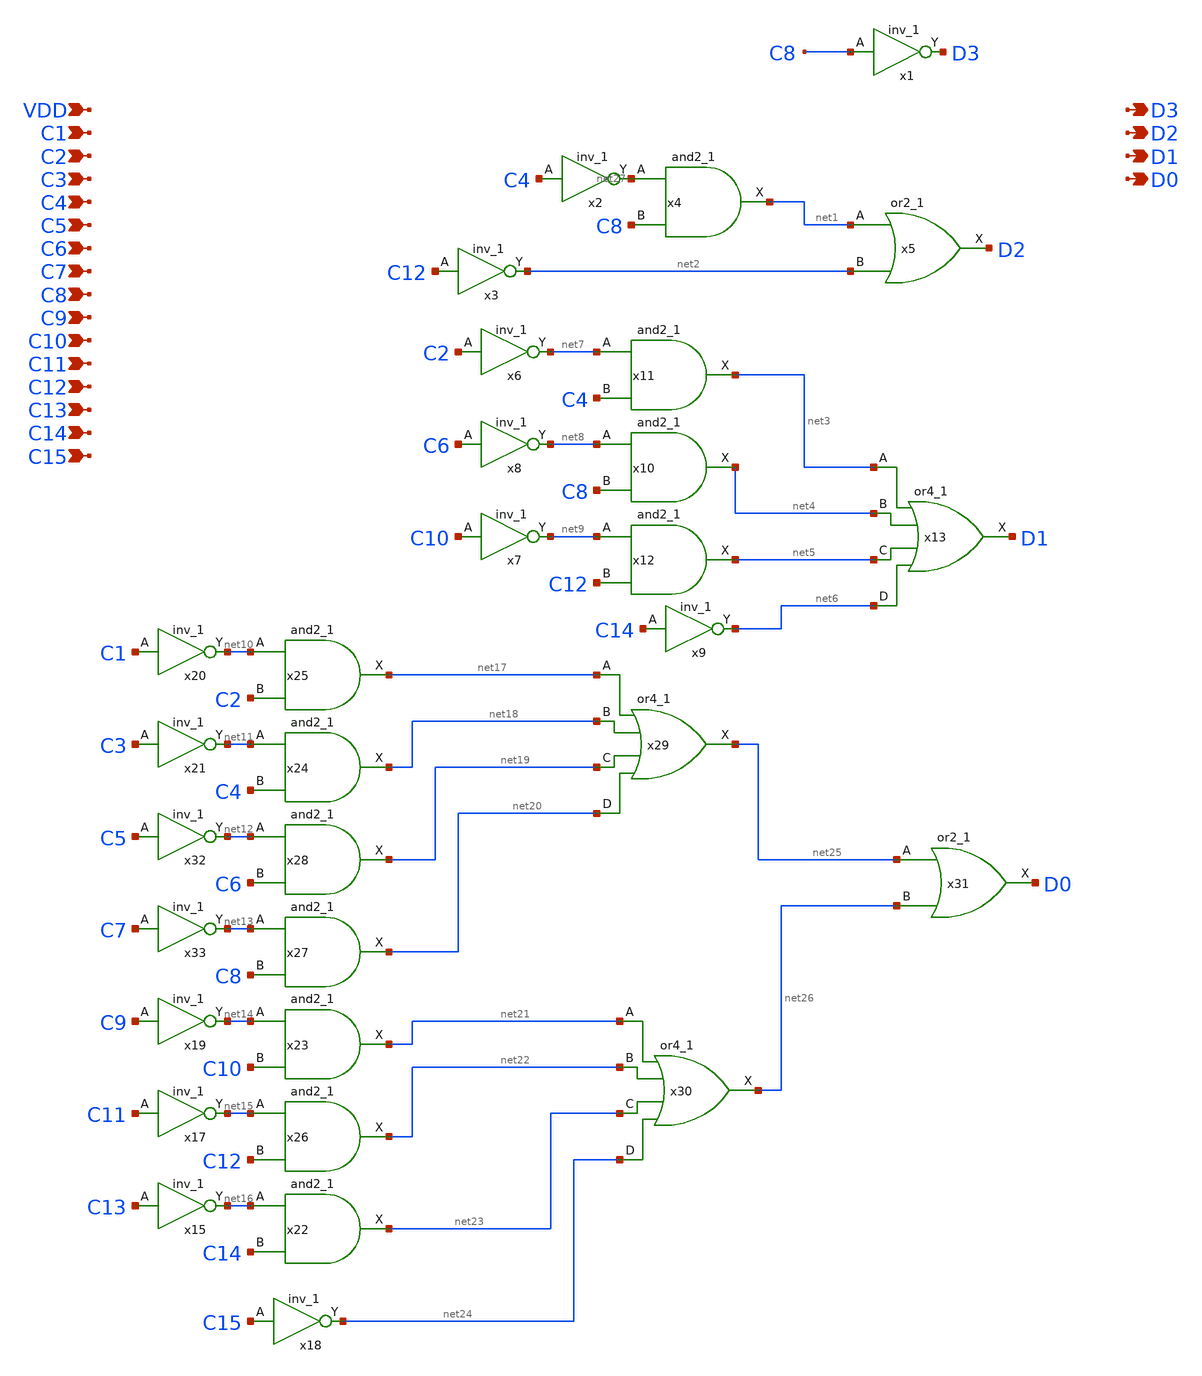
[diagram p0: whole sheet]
** sch_path: thermometer_encoder.sch
**.subckt thermometer_encoder C1 D0 C2 C3 C4 C5 C6 C7 C8 C9 C10 C11 C12 C13 C14 C15 D1 D2 D3 VDD
*.ipin C1
*.opin D0
*.ipin C2
*.ipin C3
*.ipin C4
*.ipin C5
*.ipin C6
*.ipin C7
*.ipin C8
*.ipin C9
*.ipin C10
*.ipin C11
*.ipin C12
*.ipin C13
*.ipin C14
*.ipin C15
*.opin D1
*.opin D2
*.opin D3
*.ipin VDD
x1 C8 0 0 VDD VDD D3 sky130_fd_sc_hd__inv_1
x2 C4 0 0 VDD VDD net27 sky130_fd_sc_hd__inv_1
x3 C12 0 0 VDD VDD net2 sky130_fd_sc_hd__inv_1
x4 net27 C8 0 0 VDD VDD net1 sky130_fd_sc_hd__and2_1
x5 net1 net2 0 0 VDD VDD D2 sky130_fd_sc_hd__or2_1
x6 C2 0 0 VDD VDD net7 sky130_fd_sc_hd__inv_1
x7 C10 0 0 VDD VDD net9 sky130_fd_sc_hd__inv_1
x8 C6 0 0 VDD VDD net8 sky130_fd_sc_hd__inv_1
x9 C14 0 0 VDD VDD net6 sky130_fd_sc_hd__inv_1
x12 net9 C12 0 0 VDD VDD net5 sky130_fd_sc_hd__and2_1
x13 net3 net4 net5 net6 0 0 VDD VDD D1 sky130_fd_sc_hd__or4_1
x10 net8 C8 0 0 VDD VDD net4 sky130_fd_sc_hd__and2_1
x11 net7 C4 0 0 VDD VDD net3 sky130_fd_sc_hd__and2_1
x15 C13 0 0 VDD VDD net16 sky130_fd_sc_hd__inv_1
x17 C11 0 0 VDD VDD net15 sky130_fd_sc_hd__inv_1
x18 C15 0 0 VDD VDD net24 sky130_fd_sc_hd__inv_1
x19 C9 0 0 VDD VDD net14 sky130_fd_sc_hd__inv_1
x20 C1 0 0 VDD VDD net10 sky130_fd_sc_hd__inv_1
x21 C3 0 0 VDD VDD net11 sky130_fd_sc_hd__inv_1
x22 net16 C14 0 0 VDD VDD net23 sky130_fd_sc_hd__and2_1
x23 net14 C10 0 0 VDD VDD net21 sky130_fd_sc_hd__and2_1
x24 net11 C4 0 0 VDD VDD net18 sky130_fd_sc_hd__and2_1
x25 net10 C2 0 0 VDD VDD net17 sky130_fd_sc_hd__and2_1
x26 net15 C12 0 0 VDD VDD net22 sky130_fd_sc_hd__and2_1
x27 net13 C8 0 0 VDD VDD net20 sky130_fd_sc_hd__and2_1
x28 net12 C6 0 0 VDD VDD net19 sky130_fd_sc_hd__and2_1
x29 net17 net18 net19 net20 0 0 VDD VDD net25 sky130_fd_sc_hd__or4_1
x30 net21 net22 net23 net24 0 0 VDD VDD net26 sky130_fd_sc_hd__or4_1
x31 net25 net26 0 0 VDD VDD D0 sky130_fd_sc_hd__or2_1
x32 C5 0 0 VDD VDD net12 sky130_fd_sc_hd__inv_1
x33 C7 0 0 VDD VDD net13 sky130_fd_sc_hd__inv_1
**.ends
.end
